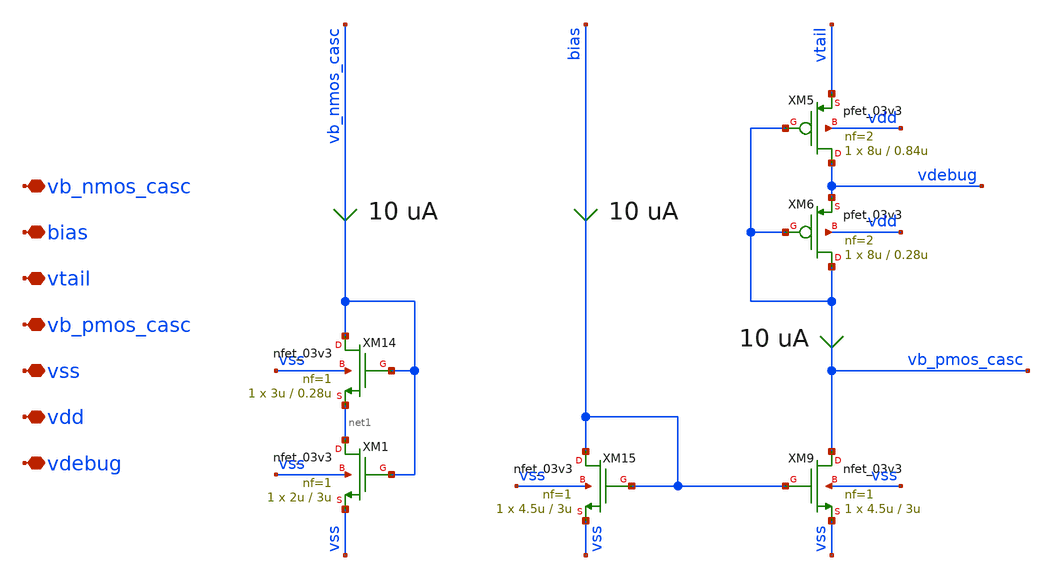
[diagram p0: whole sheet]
** sch_path: xschem/ccia_rrl_ota/b9_ccia_rrl_ota_cascode_bias.sch
**.subckt b9_ccia_rrl_ota_cascode_bias vb_nmos_casc bias vtail vb_pmos_casc vss vdd vdebug
*.iopin vb_nmos_casc
*.iopin bias
*.iopin vtail
*.iopin vb_pmos_casc
*.iopin vss
*.iopin vdd
*.iopin vdebug
XM1 net1 vb_nmos_casc vss vss nfet_03v3 L=3u W=2u nf=1 ad='int((nf+1)/2) * W/nf * 0.18u' as='int((nf+2)/2) * W/nf * 0.18u'
+ pd='2*int((nf+1)/2) * (W/nf + 0.18u)' ps='2*int((nf+2)/2) * (W/nf + 0.18u)' nrd='0.18u / W' nrs='0.18u / W'
+ sa=0 sb=0 sd=0 m=1
XM5 vdebug vb_pmos_casc vtail vdd pfet_03v3 L=0.84u W=8u nf=2 ad='int((nf+1)/2) * W/nf * 0.18u' as='int((nf+2)/2) * W/nf * 0.18u'
+ pd='2*int((nf+1)/2) * (W/nf + 0.18u)' ps='2*int((nf+2)/2) * (W/nf + 0.18u)' nrd='0.18u / W' nrs='0.18u / W'
+ sa=0 sb=0 sd=0 m=1
XM15 bias bias vss vss nfet_03v3 L=3u W=4.5u nf=1 ad='int((nf+1)/2) * W/nf * 0.18u' as='int((nf+2)/2) * W/nf * 0.18u'
+ pd='2*int((nf+1)/2) * (W/nf + 0.18u)' ps='2*int((nf+2)/2) * (W/nf + 0.18u)' nrd='0.18u / W' nrs='0.18u / W'
+ sa=0 sb=0 sd=0 m=1
XM9 vb_pmos_casc bias vss vss nfet_03v3 L=3u W=4.5u nf=1 ad='int((nf+1)/2) * W/nf * 0.18u' as='int((nf+2)/2) * W/nf * 0.18u'
+ pd='2*int((nf+1)/2) * (W/nf + 0.18u)' ps='2*int((nf+2)/2) * (W/nf + 0.18u)' nrd='0.18u / W' nrs='0.18u / W'
+ sa=0 sb=0 sd=0 m=1
XM6 vb_pmos_casc vb_pmos_casc vdebug vdd pfet_03v3 L=0.28u W=8u nf=2 ad='int((nf+1)/2) * W/nf * 0.18u'
+ as='int((nf+2)/2) * W/nf * 0.18u' pd='2*int((nf+1)/2) * (W/nf + 0.18u)' ps='2*int((nf+2)/2) * (W/nf + 0.18u)'
+ nrd='0.18u / W' nrs='0.18u / W' sa=0 sb=0 sd=0 m=1
XM14 vb_nmos_casc vb_nmos_casc net1 vss nfet_03v3 L=0.28u W=3u nf=1 ad='int((nf+1)/2) * W/nf * 0.18u'
+ as='int((nf+2)/2) * W/nf * 0.18u' pd='2*int((nf+1)/2) * (W/nf + 0.18u)' ps='2*int((nf+2)/2) * (W/nf + 0.18u)'
+ nrd='0.18u / W' nrs='0.18u / W' sa=0 sb=0 sd=0 m=1
**.ends
.end
